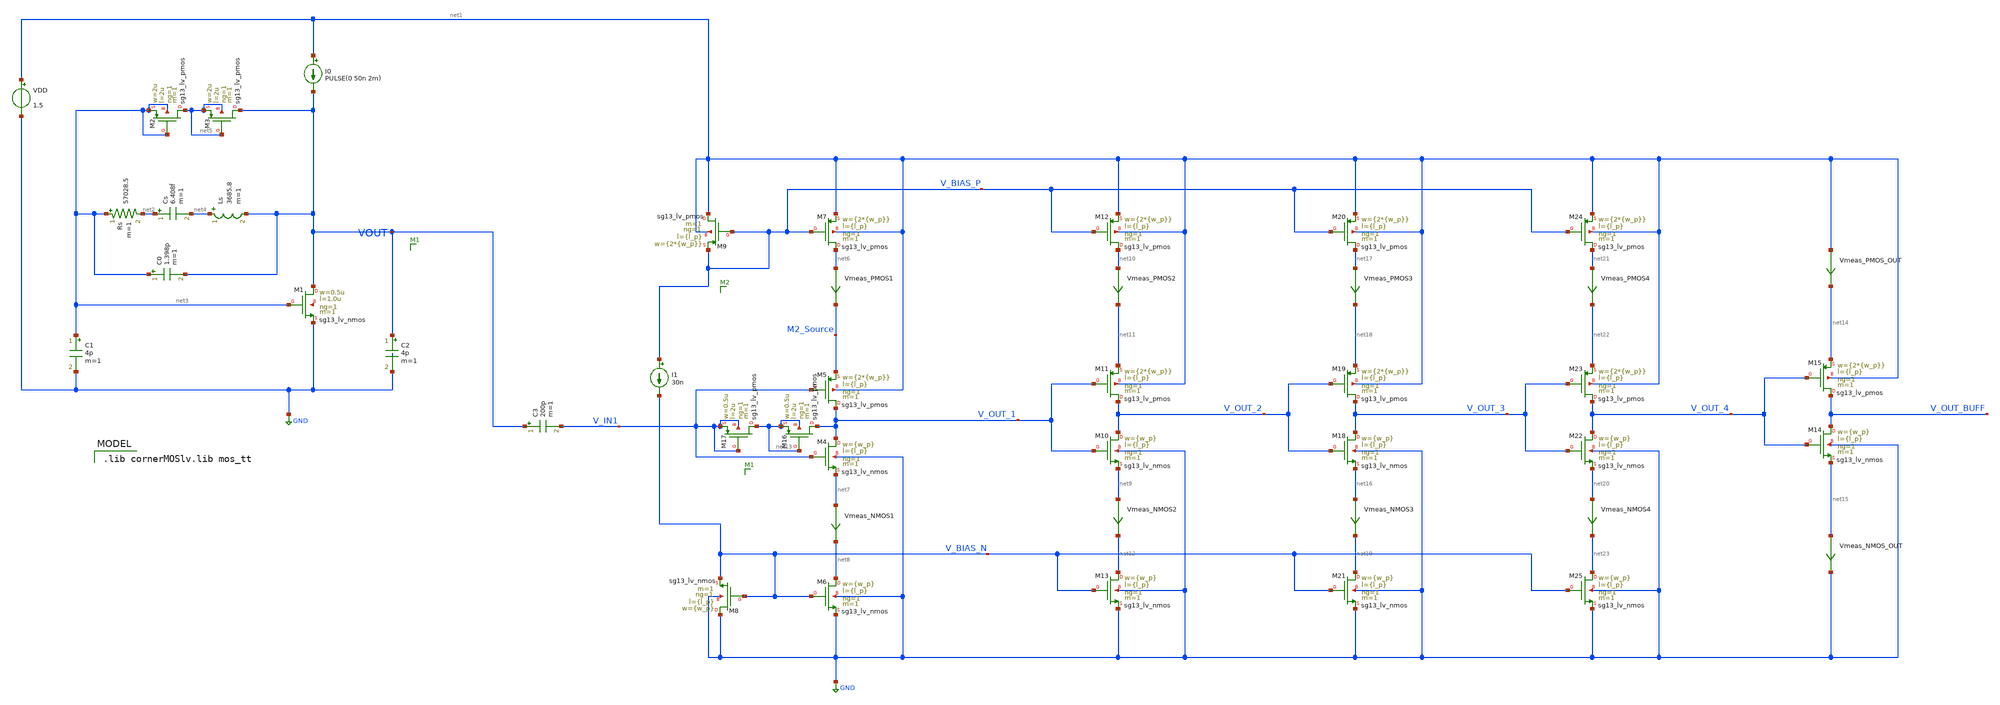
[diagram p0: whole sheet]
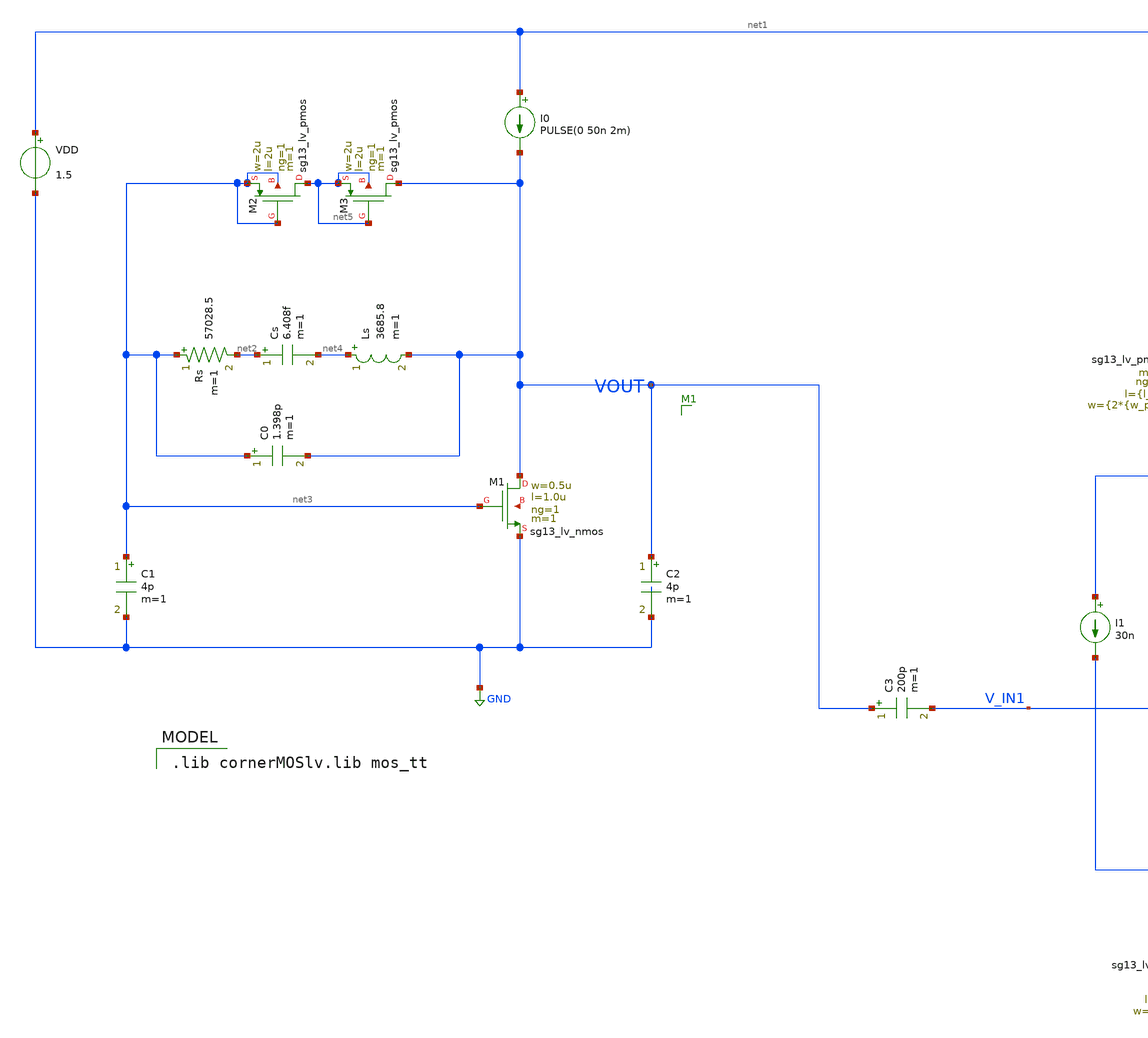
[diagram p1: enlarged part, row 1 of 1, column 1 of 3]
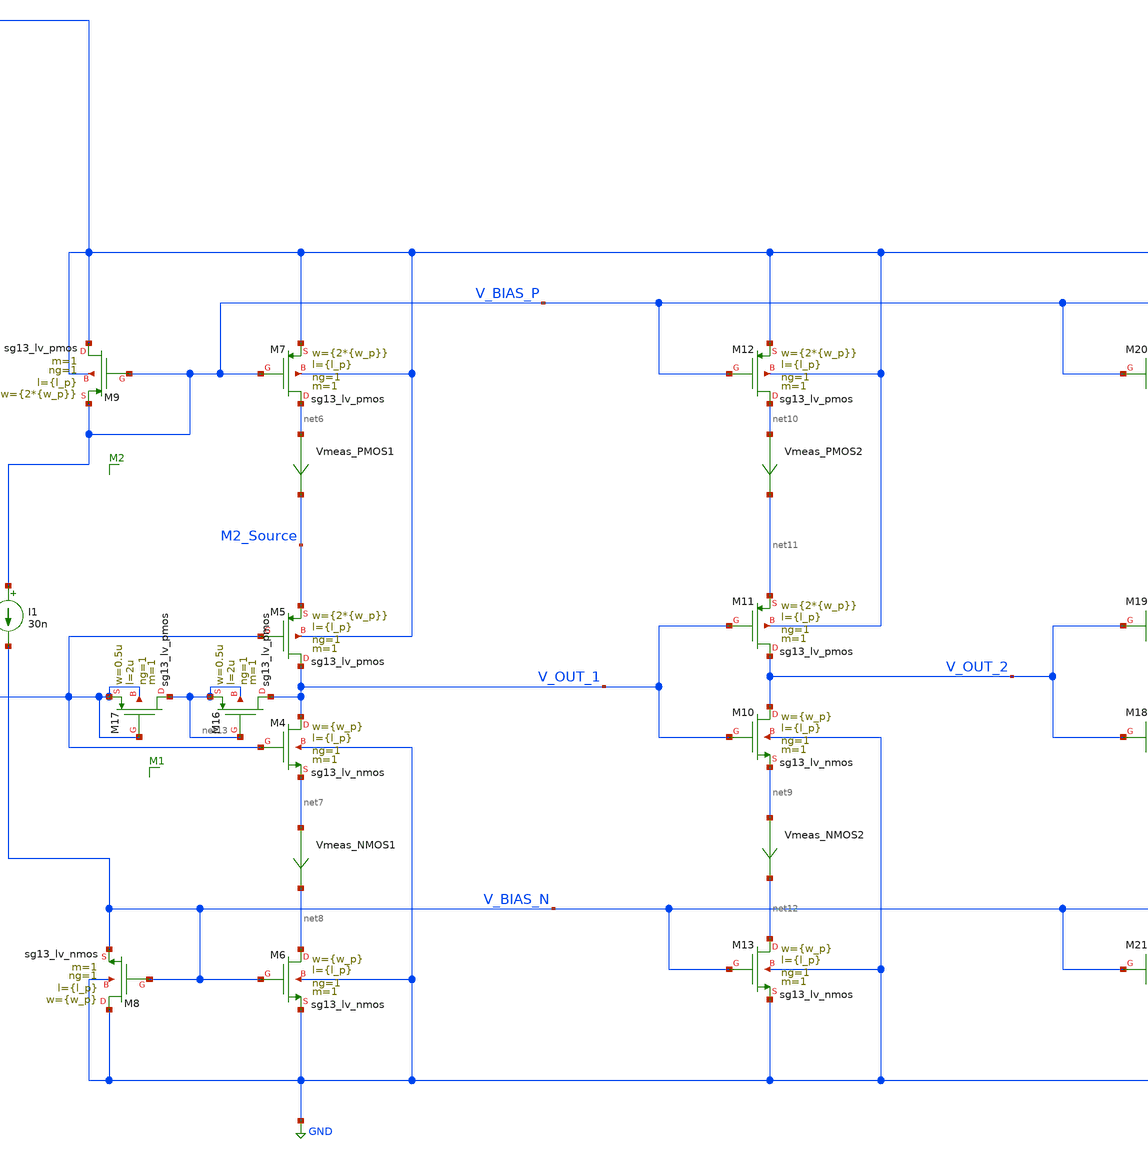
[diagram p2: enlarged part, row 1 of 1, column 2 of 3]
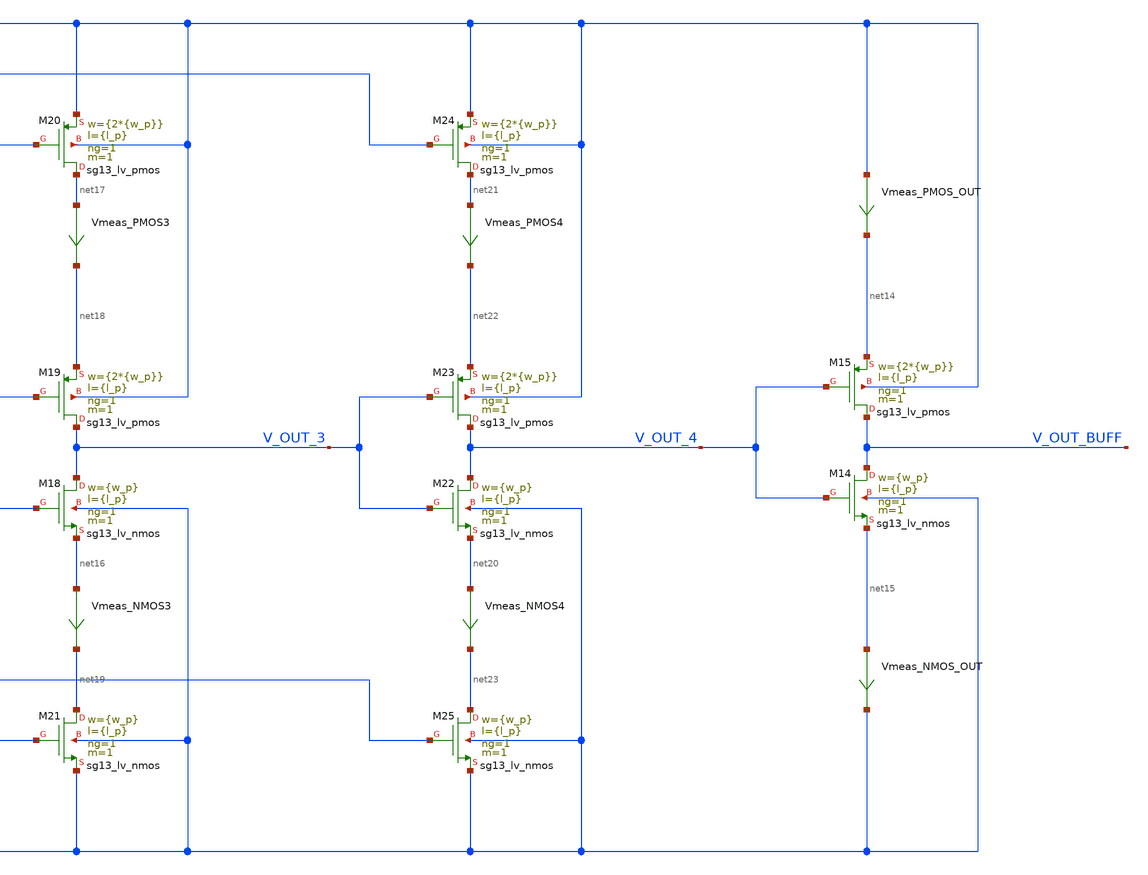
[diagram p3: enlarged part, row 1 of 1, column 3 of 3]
** sch_path: osc_core_transient_v1_tb.sch
**.subckt osc_core_transient_v1_tb
XM1 VOUT net3 GND net24 sg13_lv_nmos w=0.5u l=1.0u ng=1 m=1 mm_ok=1
C1 net3 GND 4p m=1
C2 VOUT GND 4p m=1
I0 net1 VOUT PULSE(0 50n 2m)
Rs net3 net2 57028.5 m=1
Cs net2 net4 6.408f m=1
C0 net3 VOUT 1.398p m=1
Ls net4 VOUT 3685.8 m=1
VDD net1 GND 1.5
XM2 net5 net3 net3 net3 sg13_lv_pmos w=2u l=2u ng=1 m=1 mm_ok=1
XM3 VOUT net5 net5 net5 sg13_lv_pmos w=2u l=2u ng=1 m=1 mm_ok=1
XM4 V_OUT_1 V_IN1 net7 GND sg13_lv_nmos w={w_p} l={l_p} ng=1 m=1 mm_ok=1
XM5 V_OUT_1 V_IN1 M2_Source net1 sg13_lv_pmos w={2*{w_p}} l={l_p} ng=1 m=1 mm_ok=1
XM6 net8 V_BIAS_N GND GND sg13_lv_nmos w={w_p} l={l_p} ng=1 m=1 mm_ok=1
XM7 net6 V_BIAS_P net1 net1 sg13_lv_pmos w={2*{w_p}} l={l_p} ng=1 m=1 mm_ok=1
XM8 GND V_BIAS_N V_BIAS_N GND sg13_lv_nmos w={w_p} l={l_p} ng=1 m=1 mm_ok=1
XM9 net1 V_BIAS_P V_BIAS_P net1 sg13_lv_pmos w={2*{w_p}} l={l_p} ng=1 m=1 mm_ok=1
I1 V_BIAS_P V_BIAS_N 30n
Vmeas_PMOS1 net6 M2_Source 0
.save i(vmeas_pmos1)
Vmeas_NMOS1 net7 net8 0
.save i(vmeas_nmos1)
C3 VOUT V_IN1 200p m=1
XM10 V_OUT_2 V_OUT_1 net9 GND sg13_lv_nmos w={w_p} l={l_p} ng=1 m=1 mm_ok=1
XM11 V_OUT_2 V_OUT_1 net11 net1 sg13_lv_pmos w={2*{w_p}} l={l_p} ng=1 m=1 mm_ok=1
Vmeas_NMOS2 net9 net12 0
.save i(vmeas_nmos2)
XM12 net10 V_BIAS_P net1 net1 sg13_lv_pmos w={2*{w_p}} l={l_p} ng=1 m=1 mm_ok=1
Vmeas_PMOS2 net10 net11 0
.save i(vmeas_pmos2)
XM13 net12 V_BIAS_N GND GND sg13_lv_nmos w={w_p} l={l_p} ng=1 m=1 mm_ok=1
XM14 V_OUT_BUFF V_OUT_4 net15 GND sg13_lv_nmos w={w_p} l={l_p} ng=1 m=1 mm_ok=1
XM15 V_OUT_BUFF V_OUT_4 net14 net1 sg13_lv_pmos w={2*{w_p}} l={l_p} ng=1 m=1 mm_ok=1
XM16 V_OUT_1 net13 net13 net13 sg13_lv_pmos w=0.5u l=2u ng=1 m=1 mm_ok=1
XM17 net13 V_IN1 V_IN1 V_IN1 sg13_lv_pmos w=0.5u l=2u ng=1 m=1 mm_ok=1
Vmeas_PMOS_OUT net1 net14 0
.save i(vmeas_pmos_out)
Vmeas_NMOS_OUT net15 GND 0
.save i(vmeas_nmos_out)
XM18 V_OUT_3 V_OUT_2 net16 GND sg13_lv_nmos w={w_p} l={l_p} ng=1 m=1 mm_ok=1
XM19 V_OUT_3 V_OUT_2 net18 net1 sg13_lv_pmos w={2*{w_p}} l={l_p} ng=1 m=1 mm_ok=1
Vmeas_NMOS3 net16 net19 0
.save i(vmeas_nmos3)
XM20 net17 V_BIAS_P net1 net1 sg13_lv_pmos w={2*{w_p}} l={l_p} ng=1 m=1 mm_ok=1
Vmeas_PMOS3 net17 net18 0
.save i(vmeas_pmos3)
XM21 net19 V_BIAS_N GND GND sg13_lv_nmos w={w_p} l={l_p} ng=1 m=1 mm_ok=1
XM22 V_OUT_4 V_OUT_3 net20 GND sg13_lv_nmos w={w_p} l={l_p} ng=1 m=1 mm_ok=1
XM23 V_OUT_4 V_OUT_3 net22 net1 sg13_lv_pmos w={2*{w_p}} l={l_p} ng=1 m=1 mm_ok=1
Vmeas_NMOS4 net20 net23 0
.save i(vmeas_nmos4)
XM24 net21 V_BIAS_P net1 net1 sg13_lv_pmos w={2*{w_p}} l={l_p} ng=1 m=1 mm_ok=1
Vmeas_PMOS4 net21 net22 0
.save i(vmeas_pmos4)
XM25 net23 V_BIAS_N GND GND sg13_lv_nmos w={w_p} l={l_p} ng=1 m=1 mm_ok=1
**** begin user architecture code


.param w_p=0.45u l_p=0.13u
.control
save VOUT V_OUT_BUFF

tran 0.01m 0.5s
plot VOUT V_OUT_BUFF
*setplot tran1
*linearize VOUT
*set specwindow=blackman
*fft VOUT
*plot mag(VOUT)

write osc_core_transient_v1_tb.raw

.endc


 .lib cornerMOSlv.lib mos_tt

**** end user architecture code
**.ends
.GLOBAL GND
.end
